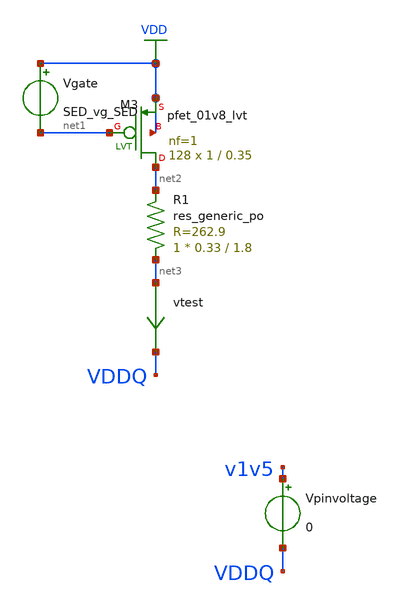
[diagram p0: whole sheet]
** sch_path: schem/test_pu_res.sch
* Copyright 2021 Stefan Frederik Schippers
* Licensed under the Apache License, Version 2.0 (the "License");
* you may not use this file except in compliance with the License.
* You may obtain a copy of the License at
* https://www.apache.org/licenses/LICENSE-2.0
* Unless required by applicable law or agreed to in writing, software
* distributed under the License is distributed on an "AS IS" BASIS,
* WITHOUT WARRANTIES OR CONDITIONS OF ANY KIND, either express or implied.
* See the License for the specific language governing permissions and
* limitations under the License.
**.subckt test_pu_res
Vgate VDD net1 SED_vg_SED
XR1 net3 net2 sky130_fd_pr__res_generic_po W=0.33 L=1.8 m=1
vtest net3 VDDQ 0
.save i(vtest)
Vpinvoltage v1v5 VDDQ 0
XM3 net2 net1 VDD VDD sky130_fd_pr__pfet_01v8_lvt L=0.35 W=1 nf=1 ad='int((nf+1)/2) * W/nf * 0.29' as='int((nf+2)/2) * W/nf * 0.29'
+ pd='2*int((nf+1)/2) * (W/nf + 0.29)' ps='2*int((nf+2)/2) * (W/nf + 0.29)' nrd='0.29 / W' nrs='0.29 / W'
+ sa=0 sb=0 sd=0 mult=128 m=128
**** begin user architecture code
 ** Local library links to pdk
.lib ./sky130/libs/SED_process_SED_lib.spice SED_process_SED

**** end user architecture code
**.ends
.GLOBAL VDD
**** begin user architecture code



* power voltage
vvdd VDD 0 SED_vdd_SED
vv1v5 v1v5 0 1.5

*.param rwidth=4.6

.control
save all
set temp=SED_temp_SED

* RUN SIMULATION
dc Vpinvoltage 0.3 1.2 0.05
* OUTPUT
print (SED_vdd_SED-vddq)/i(vtest)
wrdata out/SED_outName_SED/SED_plotName_SED.txt (SED_vdd_SED-vddq)/i(vtest)
set hcopydevtype = svg
hardcopy ./out/SED_outName_SED/SED_plotName_SED.svg (SED_vdd_SED-vddq)/I(vtest) vs vddq title 'Resistance vs pin voltage'

.endc


**** end user architecture code
.end
